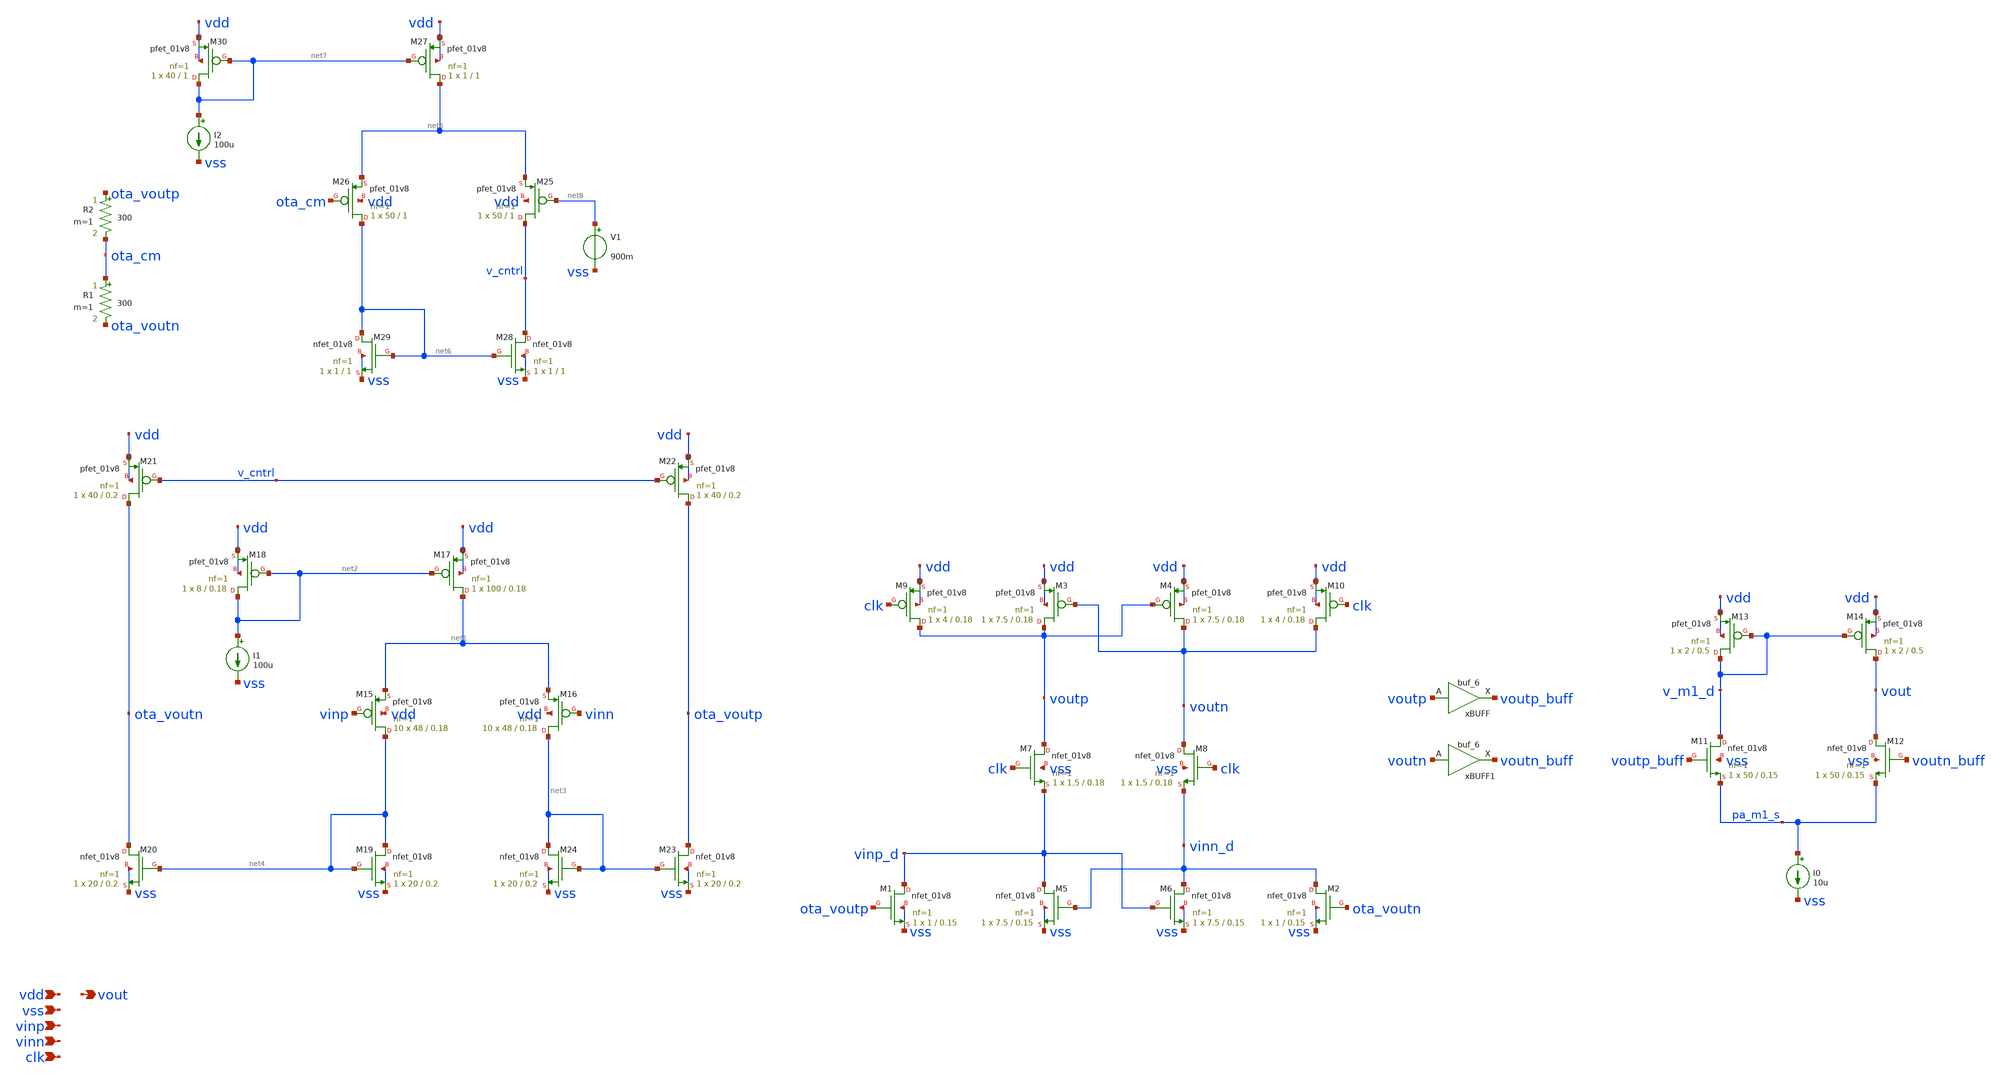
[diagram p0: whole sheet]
** sch_path: schematics/comp_5023.sch
**.subckt comp_5023 vdd vout vss vinp vinn clk
*.ipin vdd
*.opin vout
*.ipin vss
*.ipin vinp
*.ipin vinn
*.ipin clk
XM1 vinp_d ota_voutp vss vss sky130_fd_pr__nfet_01v8 L=0.15 W=1 nf=1 ad='int((1 + 1)/2) * 1 / 1 * 0.29'
+ as='int((1 + 2)/2) * 1 / 1 * 0.29' pd='2*int((1 + 1)/2) * (1 / 1 + 0.29)' ps='2*int((1 + 2)/2) * (1 / 1 + 0.29)'
+ nrd='0.29 / 1 ' nrs='0.29 / 1 ' sa=0 sb=0 sd=0 mult=1 m=1
XM2 vinn_d ota_voutn vss vss sky130_fd_pr__nfet_01v8 L=0.15 W=1 nf=1 ad='int((1 + 1)/2) * 1 / 1 * 0.29'
+ as='int((1 + 2)/2) * 1 / 1 * 0.29' pd='2*int((1 + 1)/2) * (1 / 1 + 0.29)' ps='2*int((1 + 2)/2) * (1 / 1 + 0.29)'
+ nrd='0.29 / 1 ' nrs='0.29 / 1 ' sa=0 sb=0 sd=0 mult=1 m=1
XM3 voutp voutn vdd vdd sky130_fd_pr__pfet_01v8 L=0.18 W=7.5 nf=1 ad='int((1 + 1)/2) * 7.5 / 1 * 0.29'
+ as='int((1 + 2)/2) * 7.5 / 1 * 0.29' pd='2*int((1 + 1)/2) * (7.5 / 1 + 0.29)' ps='2*int((1 + 2)/2) * (7.5 / 1 + 0.29)'
+ nrd='0.29 / 7.5 ' nrs='0.29 / 7.5 ' sa=0 sb=0 sd=0 mult=1 m=1
XM4 voutn voutp vdd vdd sky130_fd_pr__pfet_01v8 L=0.18 W=7.5 nf=1 ad='int((1 + 1)/2) * 7.5 / 1 * 0.29'
+ as='int((1 + 2)/2) * 7.5 / 1 * 0.29' pd='2*int((1 + 1)/2) * (7.5 / 1 + 0.29)' ps='2*int((1 + 2)/2) * (7.5 / 1 + 0.29)'
+ nrd='0.29 / 7.5 ' nrs='0.29 / 7.5 ' sa=0 sb=0 sd=0 mult=1 m=1
XM5 vinp_d vinn_d vss vss sky130_fd_pr__nfet_01v8 L=0.15 W=7.5 nf=1 ad='int((1 + 1)/2) * 7.5 / 1 * 0.29'
+ as='int((1 + 2)/2) * 7.5 / 1 * 0.29' pd='2*int((1 + 1)/2) * (7.5 / 1 + 0.29)' ps='2*int((1 + 2)/2) * (7.5 / 1 + 0.29)'
+ nrd='0.29 / 7.5 ' nrs='0.29 / 7.5 ' sa=0 sb=0 sd=0 mult=1 m=1
XM6 vinn_d vinp_d vss vss sky130_fd_pr__nfet_01v8 L=0.15 W=7.5 nf=1 ad='int((1 + 1)/2) * 7.5 / 1 * 0.29'
+ as='int((1 + 2)/2) * 7.5 / 1 * 0.29' pd='2*int((1 + 1)/2) * (7.5 / 1 + 0.29)' ps='2*int((1 + 2)/2) * (7.5 / 1 + 0.29)'
+ nrd='0.29 / 7.5 ' nrs='0.29 / 7.5 ' sa=0 sb=0 sd=0 mult=1 m=1
XM7 voutp clk vinp_d vss sky130_fd_pr__nfet_01v8 L=0.18 W=1.5 nf=1 ad='int((1 + 1)/2) * 1.5 / 1 * 0.29'
+ as='int((1 + 2)/2) * 1.5 / 1 * 0.29' pd='2*int((1 + 1)/2) * (1.5 / 1 + 0.29)' ps='2*int((1 + 2)/2) * (1.5 / 1 + 0.29)'
+ nrd='0.29 / 1.5 ' nrs='0.29 / 1.5 ' sa=0 sb=0 sd=0 mult=1 m=1
XM8 voutn clk vinn_d vss sky130_fd_pr__nfet_01v8 L=0.18 W=1.5 nf=1 ad='int((1 + 1)/2) * 1.5 / 1 * 0.29'
+ as='int((1 + 2)/2) * 1.5 / 1 * 0.29' pd='2*int((1 + 1)/2) * (1.5 / 1 + 0.29)' ps='2*int((1 + 2)/2) * (1.5 / 1 + 0.29)'
+ nrd='0.29 / 1.5 ' nrs='0.29 / 1.5 ' sa=0 sb=0 sd=0 mult=1 m=1
XM9 voutp clk vdd vdd sky130_fd_pr__pfet_01v8 L=0.18 W=4 nf=1 ad='int((1 + 1)/2) * 4 / 1 * 0.29' as='int((1 + 2)/2) * 4 / 1 * 0.29'
+ pd='2*int((1 + 1)/2) * (4 / 1 + 0.29)' ps='2*int((1 + 2)/2) * (4 / 1 + 0.29)' nrd='0.29 / 4 ' nrs='0.29 / 4 '
+ sa=0 sb=0 sd=0 mult=1 m=1
XM10 voutn clk vdd vdd sky130_fd_pr__pfet_01v8 L=0.18 W=4 nf=1 ad='int((1 + 1)/2) * 4 / 1 * 0.29' as='int((1 + 2)/2) * 4 / 1 * 0.29'
+ pd='2*int((1 + 1)/2) * (4 / 1 + 0.29)' ps='2*int((1 + 2)/2) * (4 / 1 + 0.29)' nrd='0.29 / 4 ' nrs='0.29 / 4 '
+ sa=0 sb=0 sd=0 mult=1 m=1
xBUFF voutp vss vss vdd vdd voutp_buff sky130_fd_sc_hd__buf_6
xBUFF1 voutn vss vss vdd vdd voutn_buff sky130_fd_sc_hd__buf_6
I0 pa_m1_s vss 10u
XM11 v_m1_d voutp_buff pa_m1_s vss sky130_fd_pr__nfet_01v8 L=0.15 W=50 nf=1 ad='int((1 + 1)/2) * 50 / 1 * 0.29'
+ as='int((1 + 2)/2) * 50 / 1 * 0.29' pd='2*int((1 + 1)/2) * (50 / 1 + 0.29)' ps='2*int((1 + 2)/2) * (50 / 1 + 0.29)'
+ nrd='0.29 / 50 ' nrs='0.29 / 50 ' sa=0 sb=0 sd=0 mult=1 m=1
XM12 vout voutn_buff pa_m1_s vss sky130_fd_pr__nfet_01v8 L=0.15 W=50 nf=1 ad='int((1 + 1)/2) * 50 / 1 * 0.29'
+ as='int((1 + 2)/2) * 50 / 1 * 0.29' pd='2*int((1 + 1)/2) * (50 / 1 + 0.29)' ps='2*int((1 + 2)/2) * (50 / 1 + 0.29)'
+ nrd='0.29 / 50 ' nrs='0.29 / 50 ' sa=0 sb=0 sd=0 mult=1 m=1
XM13 v_m1_d v_m1_d vdd vdd sky130_fd_pr__pfet_01v8 L=0.5 W=2 nf=1 ad='int((1 + 1)/2) * 2 / 1 * 0.29'
+ as='int((1 + 2)/2) * 2 / 1 * 0.29' pd='2*int((1 + 1)/2) * (2 / 1 + 0.29)' ps='2*int((1 + 2)/2) * (2 / 1 + 0.29)'
+ nrd='0.29 / 2 ' nrs='0.29 / 2 ' sa=0 sb=0 sd=0 mult=1 m=1
XM14 vout v_m1_d vdd vdd sky130_fd_pr__pfet_01v8 L=0.5 W=2 nf=1 ad='int((1 + 1)/2) * 2 / 1 * 0.29' as='int((1 + 2)/2) * 2 / 1 * 0.29'
+ pd='2*int((1 + 1)/2) * (2 / 1 + 0.29)' ps='2*int((1 + 2)/2) * (2 / 1 + 0.29)' nrd='0.29 / 2 ' nrs='0.29 / 2 '
+ sa=0 sb=0 sd=0 mult=1 m=1
XM17 net1 net2 vdd vdd sky130_fd_pr__pfet_01v8 L=0.18 W=100 nf=1 ad='int((1 + 1)/2) * 100 / 1 * 0.29'
+ as='int((1 + 2)/2) * 100 / 1 * 0.29' pd='2*int((1 + 1)/2) * (100 / 1 + 0.29)' ps='2*int((1 + 2)/2) * (100 / 1 + 0.29)'
+ nrd='0.29 / 100 ' nrs='0.29 / 100 ' sa=0 sb=0 sd=0 mult=1 m=1
XM18 net2 net2 vdd vdd sky130_fd_pr__pfet_01v8 L=0.18 W=8 nf=1 ad='int((1 + 1)/2) * 8 / 1 * 0.29' as='int((1 + 2)/2) * 8 / 1 * 0.29'
+ pd='2*int((1 + 1)/2) * (8 / 1 + 0.29)' ps='2*int((1 + 2)/2) * (8 / 1 + 0.29)' nrd='0.29 / 8 ' nrs='0.29 / 8 '
+ sa=0 sb=0 sd=0 mult=1 m=1
I1 net2 vss 100u
XM19 net4 net4 vss vss sky130_fd_pr__nfet_01v8 L=0.2 W=20 nf=1 ad='int((1 + 1)/2) * 20 / 1 * 0.29' as='int((1 + 2)/2) * 20 / 1 * 0.29'
+ pd='2*int((1 + 1)/2) * (20 / 1 + 0.29)' ps='2*int((1 + 2)/2) * (20 / 1 + 0.29)' nrd='0.29 / 20 ' nrs='0.29 / 20 '
+ sa=0 sb=0 sd=0 mult=1 m=1
XM20 ota_voutn net4 vss vss sky130_fd_pr__nfet_01v8 L=0.2 W=20 nf=1 ad='int((1 + 1)/2) * 20 / 1 * 0.29'
+ as='int((1 + 2)/2) * 20 / 1 * 0.29' pd='2*int((1 + 1)/2) * (20 / 1 + 0.29)' ps='2*int((1 + 2)/2) * (20 / 1 + 0.29)'
+ nrd='0.29 / 20 ' nrs='0.29 / 20 ' sa=0 sb=0 sd=0 mult=1 m=1
XM21 ota_voutn v_cntrl vdd vdd sky130_fd_pr__pfet_01v8 L=0.2 W=40 nf=1 ad='int((1 + 1)/2) * 40 / 1 * 0.29'
+ as='int((1 + 2)/2) * 40 / 1 * 0.29' pd='2*int((1 + 1)/2) * (40 / 1 + 0.29)' ps='2*int((1 + 2)/2) * (40 / 1 + 0.29)'
+ nrd='0.29 / 40 ' nrs='0.29 / 40 ' sa=0 sb=0 sd=0 mult=1 m=1
XM22 ota_voutp v_cntrl vdd vdd sky130_fd_pr__pfet_01v8 L=0.2 W=40 nf=1 ad='int((1 + 1)/2) * 40 / 1 * 0.29'
+ as='int((1 + 2)/2) * 40 / 1 * 0.29' pd='2*int((1 + 1)/2) * (40 / 1 + 0.29)' ps='2*int((1 + 2)/2) * (40 / 1 + 0.29)'
+ nrd='0.29 / 40 ' nrs='0.29 / 40 ' sa=0 sb=0 sd=0 mult=1 m=1
XM23 ota_voutp net3 vss vss sky130_fd_pr__nfet_01v8 L=0.2 W=20 nf=1 ad='int((1 + 1)/2) * 20 / 1 * 0.29'
+ as='int((1 + 2)/2) * 20 / 1 * 0.29' pd='2*int((1 + 1)/2) * (20 / 1 + 0.29)' ps='2*int((1 + 2)/2) * (20 / 1 + 0.29)'
+ nrd='0.29 / 20 ' nrs='0.29 / 20 ' sa=0 sb=0 sd=0 mult=1 m=1
XM24 net3 net3 vss vss sky130_fd_pr__nfet_01v8 L=0.2 W=20 nf=1 ad='int((1 + 1)/2) * 20 / 1 * 0.29' as='int((1 + 2)/2) * 20 / 1 * 0.29'
+ pd='2*int((1 + 1)/2) * (20 / 1 + 0.29)' ps='2*int((1 + 2)/2) * (20 / 1 + 0.29)' nrd='0.29 / 20 ' nrs='0.29 / 20 '
+ sa=0 sb=0 sd=0 mult=1 m=1
XM27 net5 net7 vdd vdd sky130_fd_pr__pfet_01v8 L=1 W=1 nf=1 ad='int((1 + 1)/2) * 1 / 1 * 0.29' as='int((1 + 2)/2) * 1 / 1 * 0.29'
+ pd='2*int((1 + 1)/2) * (1 / 1 + 0.29)' ps='2*int((1 + 2)/2) * (1 / 1 + 0.29)' nrd='0.29 / 1 ' nrs='0.29 / 1 '
+ sa=0 sb=0 sd=0 mult=1 m=1
XM28 v_cntrl net6 vss vss sky130_fd_pr__nfet_01v8 L=1 W=1 nf=1 ad='int((1 + 1)/2) * 1 / 1 * 0.29' as='int((1 + 2)/2) * 1 / 1 * 0.29'
+ pd='2*int((1 + 1)/2) * (1 / 1 + 0.29)' ps='2*int((1 + 2)/2) * (1 / 1 + 0.29)' nrd='0.29 / 1 ' nrs='0.29 / 1 '
+ sa=0 sb=0 sd=0 mult=1 m=1
XM29 net6 net6 vss vss sky130_fd_pr__nfet_01v8 L=1 W=1 nf=1 ad='int((1 + 1)/2) * 1 / 1 * 0.29' as='int((1 + 2)/2) * 1 / 1 * 0.29'
+ pd='2*int((1 + 1)/2) * (1 / 1 + 0.29)' ps='2*int((1 + 2)/2) * (1 / 1 + 0.29)' nrd='0.29 / 1 ' nrs='0.29 / 1 '
+ sa=0 sb=0 sd=0 mult=1 m=1
XM25 v_cntrl net8 net5 vdd sky130_fd_pr__pfet_01v8 L=1 W=50 nf=1 ad='int((1 + 1)/2) * 50 / 1 * 0.29'
+ as='int((1 + 2)/2) * 50 / 1 * 0.29' pd='2*int((1 + 1)/2) * (50 / 1 + 0.29)' ps='2*int((1 + 2)/2) * (50 / 1 + 0.29)'
+ nrd='0.29 / 50 ' nrs='0.29 / 50 ' sa=0 sb=0 sd=0 mult=1 m=1
XM26 net6 ota_cm net5 vdd sky130_fd_pr__pfet_01v8 L=1 W=50 nf=1 ad='int((1 + 1)/2) * 50 / 1 * 0.29' as='int((1 + 2)/2) * 50 / 1 * 0.29'
+ pd='2*int((1 + 1)/2) * (50 / 1 + 0.29)' ps='2*int((1 + 2)/2) * (50 / 1 + 0.29)' nrd='0.29 / 50 ' nrs='0.29 / 50 '
+ sa=0 sb=0 sd=0 mult=1 m=1
XM30 net7 net7 vdd vdd sky130_fd_pr__pfet_01v8 L=1 W=40 nf=1 ad='int((1 + 1)/2) * 40 / 1 * 0.29' as='int((1 + 2)/2) * 40 / 1 * 0.29'
+ pd='2*int((1 + 1)/2) * (40 / 1 + 0.29)' ps='2*int((1 + 2)/2) * (40 / 1 + 0.29)' nrd='0.29 / 40 ' nrs='0.29 / 40 '
+ sa=0 sb=0 sd=0 mult=1 m=1
I2 net7 vss 100u
XM15 net4 vinp net1 vdd sky130_fd_pr__pfet_01v8 L=0.18 W=48 nf=1 ad='int((1 + 1)/2) * 48 / 1 * 0.29'
+ as='int((1 + 2)/2) * 48 / 1 * 0.29' pd='2*int((1 + 1)/2) * (48 / 1 + 0.29)' ps='2*int((1 + 2)/2) * (48 / 1 + 0.29)'
+ nrd='0.29 / 48 ' nrs='0.29 / 48 ' sa=0 sb=0 sd=0 mult=10 m=10
XM16 net3 vinn net1 vdd sky130_fd_pr__pfet_01v8 L=0.18 W=48 nf=1 ad='int((1 + 1)/2) * 48 / 1 * 0.29'
+ as='int((1 + 2)/2) * 48 / 1 * 0.29' pd='2*int((1 + 1)/2) * (48 / 1 + 0.29)' ps='2*int((1 + 2)/2) * (48 / 1 + 0.29)'
+ nrd='0.29 / 48 ' nrs='0.29 / 48 ' sa=0 sb=0 sd=0 mult=10 m=10
V1 net8 vss 900m
R1 ota_cm ota_voutn 300 m=1
R2 ota_voutp ota_cm 300 m=1
**.ends
.end
